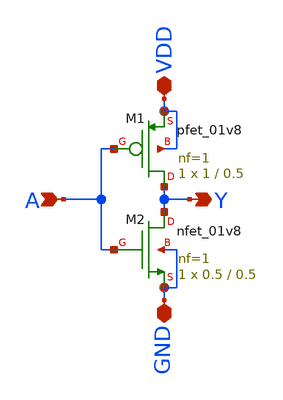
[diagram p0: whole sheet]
** sch_path: Inv.sch
**.subckt Inv A GND VDD Y
*.ipin A
*.iopin GND
*.iopin VDD
*.opin Y
XM1 Y A VDD VDD sky130_fd_pr__pfet_01v8 L=0.5 W=1 nf=1 ad='int((nf+1)/2) * W/nf * 0.29' as='int((nf+2)/2) * W/nf * 0.29'
+ pd='2*int((nf+1)/2) * (W/nf + 0.29)' ps='2*int((nf+2)/2) * (W/nf + 0.29)' nrd='0.29 / W' nrs='0.29 / W'
+ sa=0 sb=0 sd=0 mult=1 m=1
XM2 Y A GND GND sky130_fd_pr__nfet_01v8 L=0.5 W=0.5 nf=1 ad='int((nf+1)/2) * W/nf * 0.29' as='int((nf+2)/2) * W/nf * 0.29'
+ pd='2*int((nf+1)/2) * (W/nf + 0.29)' ps='2*int((nf+2)/2) * (W/nf + 0.29)' nrd='0.29 / W' nrs='0.29 / W'
+ sa=0 sb=0 sd=0 mult=1 m=1
**.ends
.end
